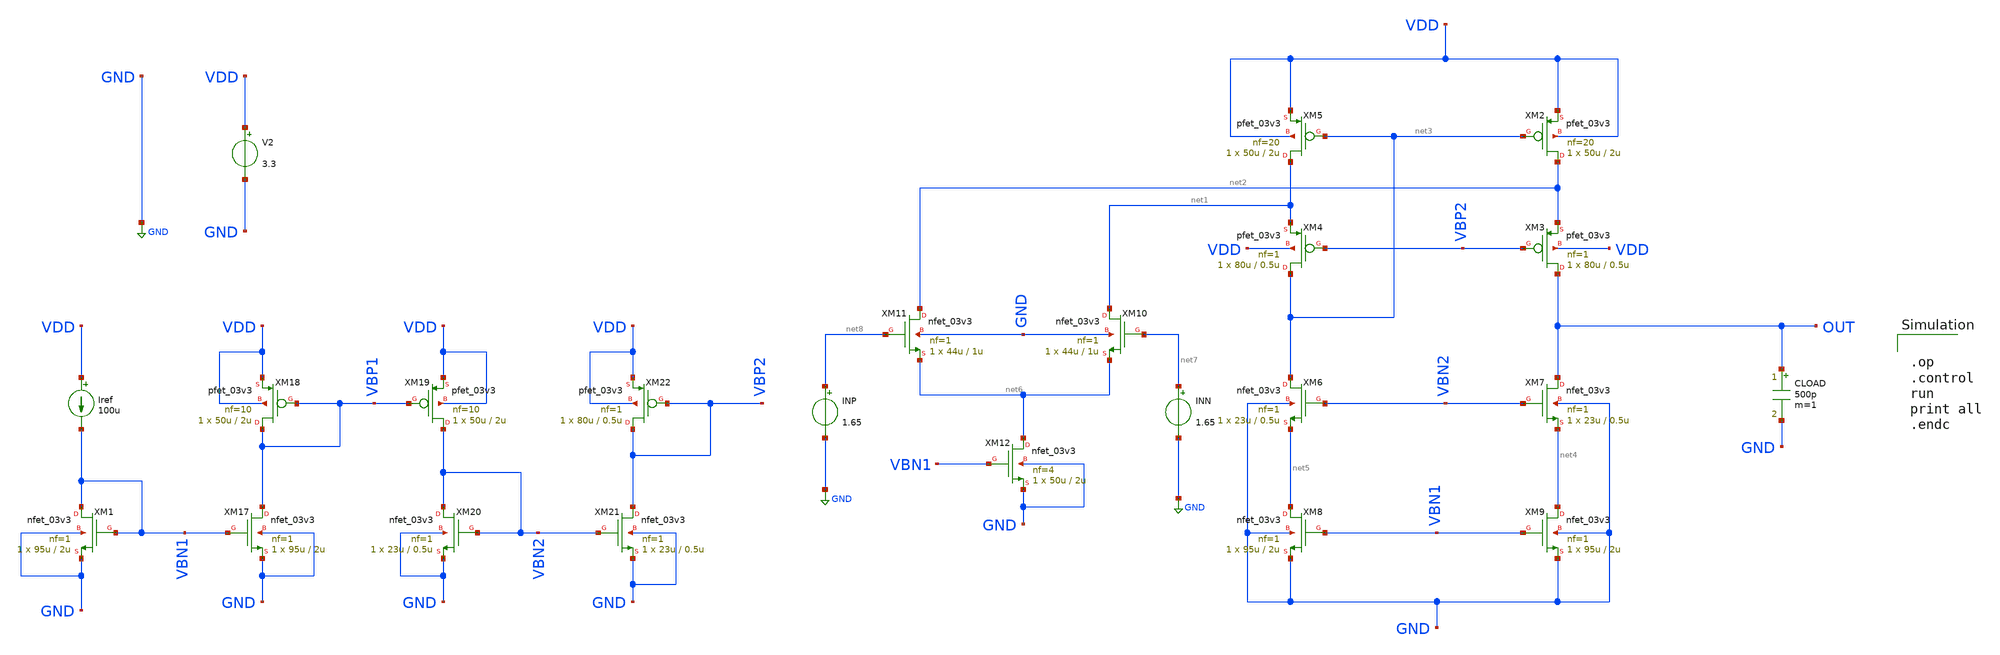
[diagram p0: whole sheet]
** sch_path: designs/libs/core_amps/ota_folded_cascode/folded.sch
**.subckt folded
Iref VDD VBN1 100u
V2 VDD GND 3.3
XM1 VBN1 VBN1 GND GND nfet_03v3 L=2u W=95u nf=1 ad='int((nf+1)/2) * W/nf * 0.18u' as='int((nf+2)/2) * W/nf * 0.18u'
+ pd='2*int((nf+1)/2) * (W/nf + 0.18u)' ps='2*int((nf+2)/2) * (W/nf + 0.18u)' nrd='0.18u / W' nrs='0.18u / W'
+ sa=0 sb=0 sd=0 m=1
XM2 net2 net3 VDD VDD pfet_03v3 L=2u W=50u nf=20 ad='int((nf+1)/2) * W/nf * 0.18u' as='int((nf+2)/2) * W/nf * 0.18u'
+ pd='2*int((nf+1)/2) * (W/nf + 0.18u)' ps='2*int((nf+2)/2) * (W/nf + 0.18u)' nrd='0.18u / W' nrs='0.18u / W'
+ sa=0 sb=0 sd=0 m=1
XM3 OUT VBP2 net2 VDD pfet_03v3 L=0.5u W=80u nf=1 ad='int((nf+1)/2) * W/nf * 0.18u' as='int((nf+2)/2) * W/nf * 0.18u'
+ pd='2*int((nf+1)/2) * (W/nf + 0.18u)' ps='2*int((nf+2)/2) * (W/nf + 0.18u)' nrd='0.18u / W' nrs='0.18u / W'
+ sa=0 sb=0 sd=0 m=1
XM4 net3 VBP2 net1 VDD pfet_03v3 L=0.5u W=80u nf=1 ad='int((nf+1)/2) * W/nf * 0.18u' as='int((nf+2)/2) * W/nf * 0.18u'
+ pd='2*int((nf+1)/2) * (W/nf + 0.18u)' ps='2*int((nf+2)/2) * (W/nf + 0.18u)' nrd='0.18u / W' nrs='0.18u / W'
+ sa=0 sb=0 sd=0 m=1
XM5 net1 net3 VDD VDD pfet_03v3 L=2u W=50u nf=20 ad='int((nf+1)/2) * W/nf * 0.18u' as='int((nf+2)/2) * W/nf * 0.18u'
+ pd='2*int((nf+1)/2) * (W/nf + 0.18u)' ps='2*int((nf+2)/2) * (W/nf + 0.18u)' nrd='0.18u / W' nrs='0.18u / W'
+ sa=0 sb=0 sd=0 m=1
XM6 net3 VBN2 net5 GND nfet_03v3 L=0.5u W=23u nf=1 ad='int((nf+1)/2) * W/nf * 0.18u' as='int((nf+2)/2) * W/nf * 0.18u'
+ pd='2*int((nf+1)/2) * (W/nf + 0.18u)' ps='2*int((nf+2)/2) * (W/nf + 0.18u)' nrd='0.18u / W' nrs='0.18u / W'
+ sa=0 sb=0 sd=0 m=1
XM7 OUT VBN2 net4 GND nfet_03v3 L=0.5u W=23u nf=1 ad='int((nf+1)/2) * W/nf * 0.18u' as='int((nf+2)/2) * W/nf * 0.18u'
+ pd='2*int((nf+1)/2) * (W/nf + 0.18u)' ps='2*int((nf+2)/2) * (W/nf + 0.18u)' nrd='0.18u / W' nrs='0.18u / W'
+ sa=0 sb=0 sd=0 m=1
XM8 net5 VBN1 GND GND nfet_03v3 L=2u W=95u nf=1 ad='int((nf+1)/2) * W/nf * 0.18u' as='int((nf+2)/2) * W/nf * 0.18u'
+ pd='2*int((nf+1)/2) * (W/nf + 0.18u)' ps='2*int((nf+2)/2) * (W/nf + 0.18u)' nrd='0.18u / W' nrs='0.18u / W'
+ sa=0 sb=0 sd=0 m=1
XM9 net4 VBN1 GND GND nfet_03v3 L=2u W=95u nf=1 ad='int((nf+1)/2) * W/nf * 0.18u' as='int((nf+2)/2) * W/nf * 0.18u'
+ pd='2*int((nf+1)/2) * (W/nf + 0.18u)' ps='2*int((nf+2)/2) * (W/nf + 0.18u)' nrd='0.18u / W' nrs='0.18u / W'
+ sa=0 sb=0 sd=0 m=1
XM10 net1 net7 net6 GND nfet_03v3 L=1u W=44u nf=1 ad='int((nf+1)/2) * W/nf * 0.18u' as='int((nf+2)/2) * W/nf * 0.18u'
+ pd='2*int((nf+1)/2) * (W/nf + 0.18u)' ps='2*int((nf+2)/2) * (W/nf + 0.18u)' nrd='0.18u / W' nrs='0.18u / W'
+ sa=0 sb=0 sd=0 m=1
XM12 net6 VBN1 GND GND nfet_03v3 L=2u W=50u nf=4 ad='int((nf+1)/2) * W/nf * 0.18u' as='int((nf+2)/2) * W/nf * 0.18u'
+ pd='2*int((nf+1)/2) * (W/nf + 0.18u)' ps='2*int((nf+2)/2) * (W/nf + 0.18u)' nrd='0.18u / W' nrs='0.18u / W'
+ sa=0 sb=0 sd=0 m=1
CLOAD OUT GND 500p m=1
XM17 VBP1 VBN1 GND GND nfet_03v3 L=2u W=95u nf=1 ad='int((nf+1)/2) * W/nf * 0.18u' as='int((nf+2)/2) * W/nf * 0.18u'
+ pd='2*int((nf+1)/2) * (W/nf + 0.18u)' ps='2*int((nf+2)/2) * (W/nf + 0.18u)' nrd='0.18u / W' nrs='0.18u / W'
+ sa=0 sb=0 sd=0 m=1
XM18 VBP1 VBP1 VDD VDD pfet_03v3 L=2u W=50u nf=10 ad='int((nf+1)/2) * W/nf * 0.18u' as='int((nf+2)/2) * W/nf * 0.18u'
+ pd='2*int((nf+1)/2) * (W/nf + 0.18u)' ps='2*int((nf+2)/2) * (W/nf + 0.18u)' nrd='0.18u / W' nrs='0.18u / W'
+ sa=0 sb=0 sd=0 m=1
XM19 VBN2 VBP1 VDD VDD pfet_03v3 L=2u W=50u nf=10 ad='int((nf+1)/2) * W/nf * 0.18u' as='int((nf+2)/2) * W/nf * 0.18u'
+ pd='2*int((nf+1)/2) * (W/nf + 0.18u)' ps='2*int((nf+2)/2) * (W/nf + 0.18u)' nrd='0.18u / W' nrs='0.18u / W'
+ sa=0 sb=0 sd=0 m=1
XM20 VBN2 VBN2 GND GND nfet_03v3 L=0.5u W=23u nf=1 ad='int((nf+1)/2) * W/nf * 0.18u' as='int((nf+2)/2) * W/nf * 0.18u'
+ pd='2*int((nf+1)/2) * (W/nf + 0.18u)' ps='2*int((nf+2)/2) * (W/nf + 0.18u)' nrd='0.18u / W' nrs='0.18u / W'
+ sa=0 sb=0 sd=0 m=1
XM21 VBP2 VBN2 GND GND nfet_03v3 L=0.5u W=23u nf=1 ad='int((nf+1)/2) * W/nf * 0.18u' as='int((nf+2)/2) * W/nf * 0.18u'
+ pd='2*int((nf+1)/2) * (W/nf + 0.18u)' ps='2*int((nf+2)/2) * (W/nf + 0.18u)' nrd='0.18u / W' nrs='0.18u / W'
+ sa=0 sb=0 sd=0 m=1
XM22 VBP2 VBP2 VDD VDD pfet_03v3 L=0.5u W=80u nf=1 ad='int((nf+1)/2) * W/nf * 0.18u' as='int((nf+2)/2) * W/nf * 0.18u'
+ pd='2*int((nf+1)/2) * (W/nf + 0.18u)' ps='2*int((nf+2)/2) * (W/nf + 0.18u)' nrd='0.18u / W' nrs='0.18u / W'
+ sa=0 sb=0 sd=0 m=1
INN net7 GND 1.65
XM11 net2 net8 net6 GND nfet_03v3 L=1u W=44u nf=1 ad='int((nf+1)/2) * W/nf * 0.18u' as='int((nf+2)/2) * W/nf * 0.18u'
+ pd='2*int((nf+1)/2) * (W/nf + 0.18u)' ps='2*int((nf+2)/2) * (W/nf + 0.18u)' nrd='0.18u / W' nrs='0.18u / W'
+ sa=0 sb=0 sd=0 m=1
INP net8 GND 1.65
**** begin user architecture code

.include $::180MCU_MODELS/design.ngspice
.lib $::180MCU_MODELS/sm141064.ngspice typical



.op
.control
run
print all
.endc



**** end user architecture code
**.ends
.GLOBAL GND
.end
